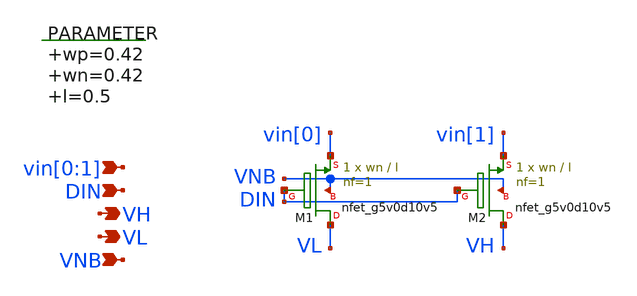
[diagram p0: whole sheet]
** sch_path: xschem/vselector_1b.sch
**.subckt vselector_1b vin[0],vin[1] VL VNB DIN VH
*.ipin vin[0],vin[1]
*.opin VL
*.ipin VNB
*.ipin DIN
*.opin VH
.param wp=0.42 wn=0.42 l=0.5

XM1 VL DIN vin[0] VNB sky130_fd_pr__nfet_g5v0d10v5 L=l W=wn nf=1 ad='int((nf+1)/2) * W/nf * 0.29' as='int((nf+2)/2) * W/nf * 0.29'
+ pd='2*int((nf+1)/2) * (W/nf + 0.29)' ps='2*int((nf+2)/2) * (W/nf + 0.29)' nrd='0.29 / W' nrs='0.29 / W'
+ sa=0 sb=0 sd=0 mult=1 m=1
XM2 VH DIN vin[1] VNB sky130_fd_pr__nfet_g5v0d10v5 L=l W=wn nf=1 ad='int((nf+1)/2) * W/nf * 0.29' as='int((nf+2)/2) * W/nf * 0.29'
+ pd='2*int((nf+1)/2) * (W/nf + 0.29)' ps='2*int((nf+2)/2) * (W/nf + 0.29)' nrd='0.29 / W' nrs='0.29 / W'
+ sa=0 sb=0 sd=0 mult=1 m=1
**.ends
.end
